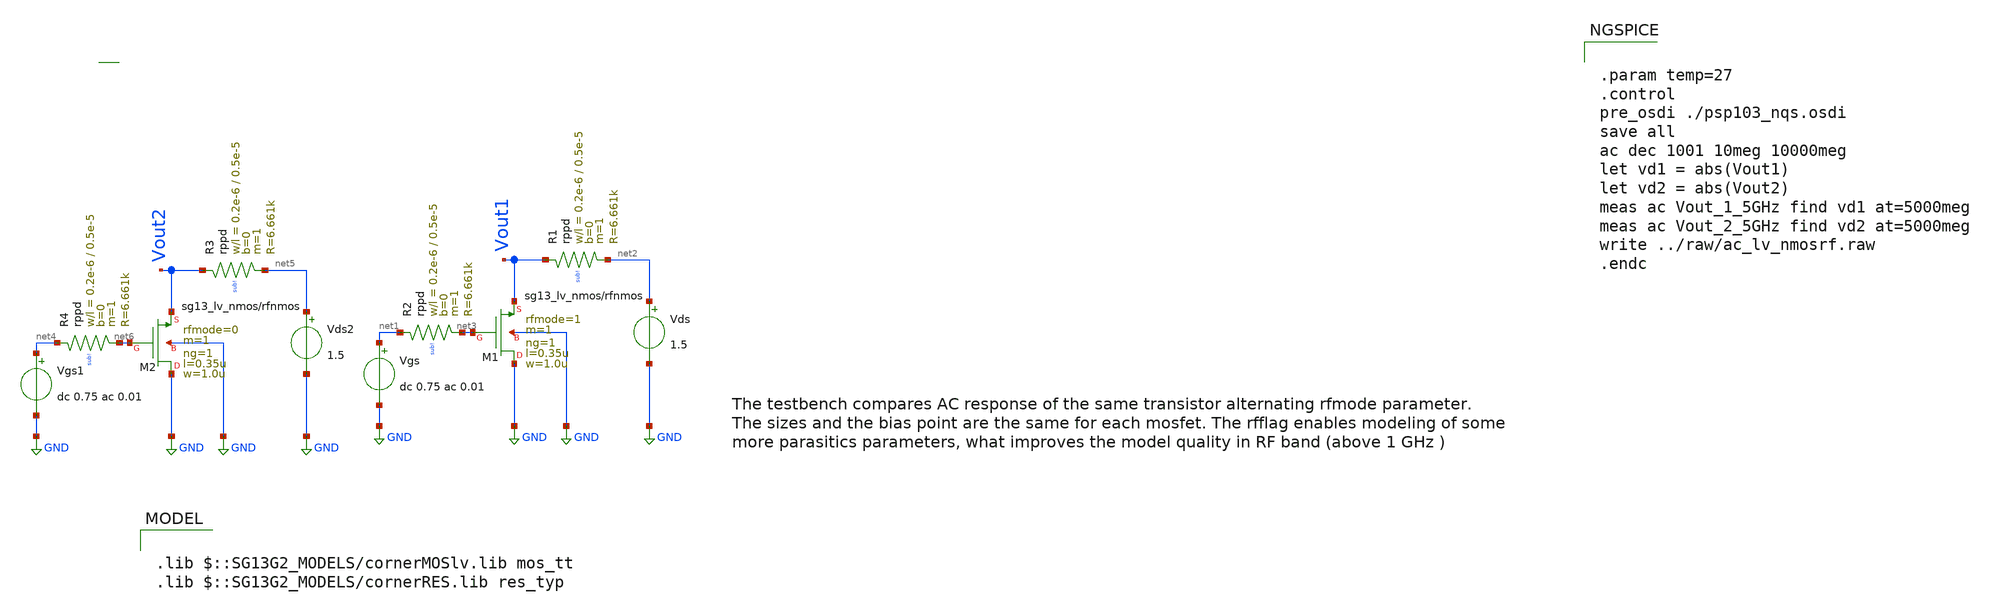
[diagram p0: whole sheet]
** sch_path: ihp-sg13g2/libs.tech/xschem/sg13g2_tests/ac_lv_nmosrf.sch
* Copyright 2023 IHP PDK Authors
**.subckt ac_lv_nmosrf
Vgs net1 GND dc 0.75 ac 0.01
Vds net2 GND 1.5
XM1 GND net3 Vout1 GND sg13_lv_nmos w=1.0u l=0.35u ng=1 m=1 rfmode=1 mm_ok=1
XR1 Vout1 net2 sub! rppd w=0.2e-6 l=0.5e-5 m=1 b=0 mm_ok=1
XR2 net1 net3 sub! rppd w=0.2e-6 l=0.5e-5 m=1 b=0 mm_ok=1
Vgs1 net4 GND dc 0.75 ac 0.01
Vds2 net5 GND 1.5
XM2 GND net6 Vout2 GND sg13_lv_nmos w=1.0u l=0.35u ng=1 m=1 rfmode=0 mm_ok=1
XR3 Vout2 net5 sub! rppd w=0.2e-6 l=0.5e-5 m=1 b=0 mm_ok=1
XR4 net4 net6 sub! rppd w=0.2e-6 l=0.5e-5 m=1 b=0 mm_ok=1
**** begin user architecture code

.lib $::SG13G2_MODELS/cornerMOSlv.lib mos_tt
.lib $::SG13G2_MODELS/cornerRES.lib res_typ



.param temp=27
.control
pre_osdi ./psp103_nqs.osdi
save all
ac dec 1001 10meg 10000meg
let vd1 = abs(Vout1)
let vd2 = abs(Vout2)
meas ac Vout_1_5GHz find vd1 at=5000meg
meas ac Vout_2_5GHz find vd2 at=5000meg
write ../raw/ac_lv_nmosrf.raw
.endc


**** end user architecture code
**.ends
.GLOBAL GND
.end
